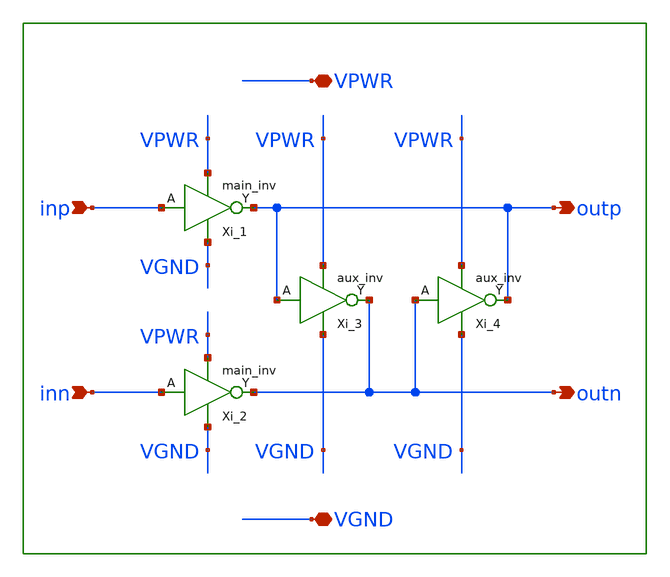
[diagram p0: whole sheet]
** sch_path: xschem/lib/cc_inv.sch
**.subckt cc_inv outp inn VGND outn inp VPWR
*.opin outp
*.ipin inn
*.iopin VGND
*.opin outn
*.ipin inp
*.iopin VPWR
Xi_1 inp VPWR VGND outp main_inv l="L_main" wp="Wp" wn="Wn"
Xi_2 inn VPWR VGND outn main_inv l="L_main" wp="Wp" wn="Wn"
Xi_3 outp VPWR VGND outn aux_inv L="L_aux" Wp="Wp" Wn="Wn"
Xi_4 outn VPWR VGND outp aux_inv L="L_aux" Wp="Wp" Wn="Wn"
**.ends

* expanding   symbol:  main_inv.sym # of pins=4
** sym_path: main_inv.sym
** sch_path: main_inv.sch
.subckt main_inv A VPWR VGND Y  l=0.15 wp=1.2 wn=0.6
*.iopin VPWR
*.iopin VGND
*.ipin A
*.opin Y
XM1 Y A VPWR VDD sky130_fd_pr__pfet_01v8 L="L" W="Wp" nf=1 ad='int((1 + 1)/2) * "Wp" / 1 * 0.29' as='int((1 + 2)/2) * "Wp" / 1 * 0.29'
+ pd='2*int((1 + 1)/2) * ("Wp" / 1 + 0.29)' ps='2*int((1 + 2)/2) * ("Wp" / 1 + 0.29)' nrd='0.29 / "Wp" '
+ nrs='0.29 / "Wp" ' sa=0 sb=0 sd=0 mult=1 m=1
XM2 Y A VGND GND sky130_fd_pr__nfet_01v8 L="L" W="Wn" nf=1 ad='int((nf+1)/2) * W/nf * 0.29' as='int((nf+2)/2) * W/nf * 0.29'
+ pd='2*int((nf+1)/2) * (W/nf + 0.29)' ps='2*int((nf+2)/2) * (W/nf + 0.29)' nrd='0.29 / W' nrs='0.29 / W'
+ sa=0 sb=0 sd=0 mult=1 m=1
XM3 Y A VPWR VDD sky130_fd_pr__pfet_01v8 L="L" W="Wp" nf=1 ad='int((1 + 1)/2) * "Wp" / 1 * 0.29' as='int((1 + 2)/2) * "Wp" / 1 * 0.29'
+ pd='2*int((1 + 1)/2) * ("Wp" / 1 + 0.29)' ps='2*int((1 + 2)/2) * ("Wp" / 1 + 0.29)' nrd='0.29 / "Wp" '
+ nrs='0.29 / "Wp" ' sa=0 sb=0 sd=0 mult=1 m=1
XM4 Y A VGND GND sky130_fd_pr__nfet_01v8 L="L" W="Wn" nf=1 ad='int((nf+1)/2) * W/nf * 0.29' as='int((nf+2)/2) * W/nf * 0.29'
+ pd='2*int((nf+1)/2) * (W/nf + 0.29)' ps='2*int((nf+2)/2) * (W/nf + 0.29)' nrd='0.29 / W' nrs='0.29 / W'
+ sa=0 sb=0 sd=0 mult=1 m=1
XM5 Y A VPWR VDD sky130_fd_pr__pfet_01v8 L="L" W="Wp" nf=1 ad='int((1 + 1)/2) * "Wp" / 1 * 0.29' as='int((1 + 2)/2) * "Wp" / 1 * 0.29'
+ pd='2*int((1 + 1)/2) * ("Wp" / 1 + 0.29)' ps='2*int((1 + 2)/2) * ("Wp" / 1 + 0.29)' nrd='0.29 / "Wp" '
+ nrs='0.29 / "Wp" ' sa=0 sb=0 sd=0 mult=1 m=1
XM6 Y A VGND GND sky130_fd_pr__nfet_01v8 L="L" W="Wn" nf=1 ad='int((nf+1)/2) * W/nf * 0.29' as='int((nf+2)/2) * W/nf * 0.29'
+ pd='2*int((nf+1)/2) * (W/nf + 0.29)' ps='2*int((nf+2)/2) * (W/nf + 0.29)' nrd='0.29 / W' nrs='0.29 / W'
+ sa=0 sb=0 sd=0 mult=1 m=1
XM7 Y A VPWR VDD sky130_fd_pr__pfet_01v8 L="L" W="Wp" nf=1 ad='int((1 + 1)/2) * "Wp" / 1 * 0.29' as='int((1 + 2)/2) * "Wp" / 1 * 0.29'
+ pd='2*int((1 + 1)/2) * ("Wp" / 1 + 0.29)' ps='2*int((1 + 2)/2) * ("Wp" / 1 + 0.29)' nrd='0.29 / "Wp" '
+ nrs='0.29 / "Wp" ' sa=0 sb=0 sd=0 mult=1 m=1
XM8 Y A VGND GND sky130_fd_pr__nfet_01v8 L="L" W="Wn" nf=1 ad='int((nf+1)/2) * W/nf * 0.29' as='int((nf+2)/2) * W/nf * 0.29'
+ pd='2*int((nf+1)/2) * (W/nf + 0.29)' ps='2*int((nf+2)/2) * (W/nf + 0.29)' nrd='0.29 / W' nrs='0.29 / W'
+ sa=0 sb=0 sd=0 mult=1 m=1
.ends


* expanding   symbol:  aux_inv.sym # of pins=4
** sym_path: xschem/lib/aux_inv.sym
** sch_path: xschem/lib/aux_inv.sch
.subckt aux_inv A VPWR VGND Y  L=0.15 Wp=1.2 Wn=0.65
*.iopin VPWR
*.iopin VGND
*.ipin A
*.opin Y
XM1 Y A VPWR VDD sky130_fd_pr__pfet_01v8 L="L" W="Wp" nf=1 ad='int((1 + 1)/2) * "Wp" / 1 * 0.29' as='int((1 + 2)/2) * "Wp" / 1 * 0.29'
+ pd='2*int((1 + 1)/2) * ("Wp" / 1 + 0.29)' ps='2*int((1 + 2)/2) * ("Wp" / 1 + 0.29)' nrd='0.29 / "Wp" '
+ nrs='0.29 / "Wp" ' sa=0 sb=0 sd=0 mult=1 m=1
XM2 Y A VGND GND sky130_fd_pr__nfet_01v8 L="L" W="Wn" nf=1 ad='int((nf+1)/2) * W/nf * 0.29' as='int((nf+2)/2) * W/nf * 0.29'
+ pd='2*int((nf+1)/2) * (W/nf + 0.29)' ps='2*int((nf+2)/2) * (W/nf + 0.29)' nrd='0.29 / W' nrs='0.29 / W'
+ sa=0 sb=0 sd=0 mult=1 m=1
.ends

.end
